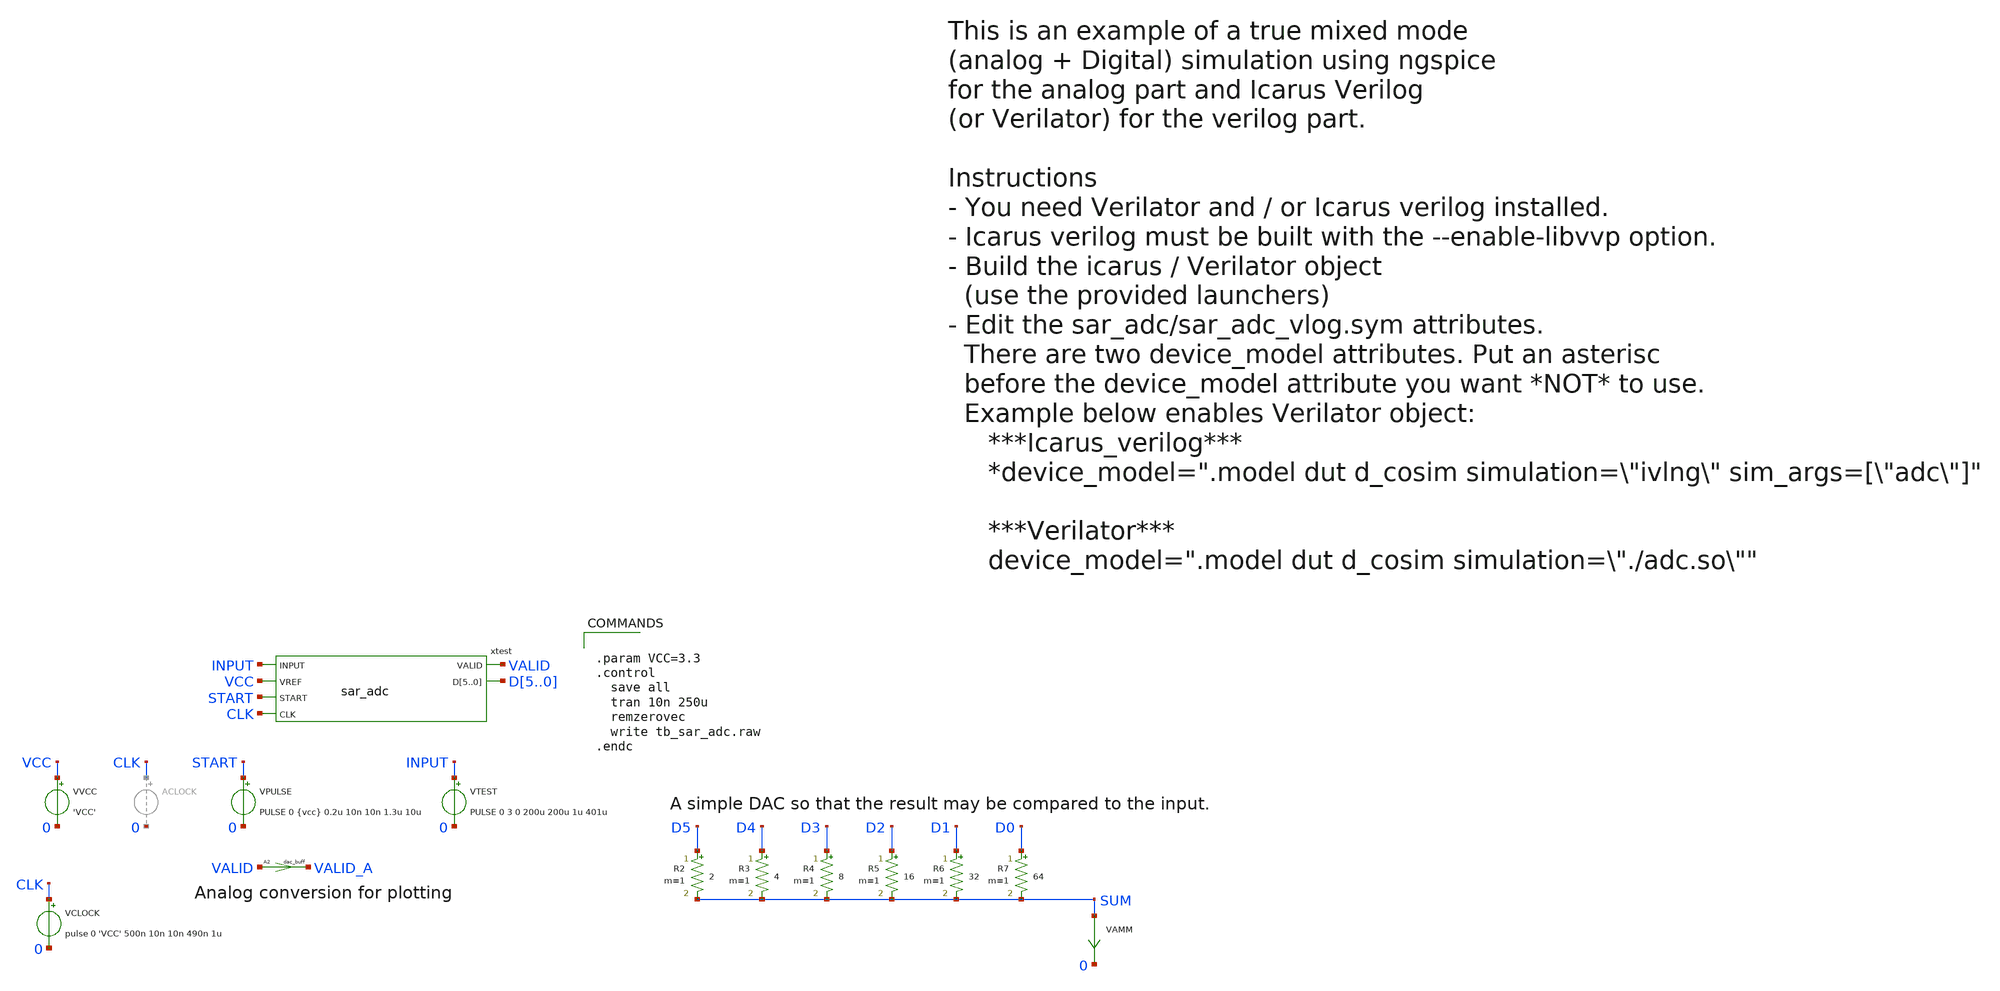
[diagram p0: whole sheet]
** sch_path: xschem_libraries_oa/ngspice_verilog_cosim/tb_sar_adc/schematic/tb_sar_adc.sch
**.subckt tb_sar_adc
VAMM SUM 0 0
VPULSE START 0 PULSE 0 {vcc} 0.2u 10n 10n 1.3u 10u
VTEST INPUT 0 PULSE 0 3 0 200u 200u 1u 401u
VVCC VCC 0 'VCC'
R2 D5 SUM 2 m=1
R3 D4 SUM 4 m=1
R4 D3 SUM 8 m=1
R5 D2 SUM 16 m=1
R6 D1 SUM 32 m=1
R7 D0 SUM 64 m=1
xtest INPUT VCC START VALID D5 D4 D3 D2 D1 D0 CLK sar_adc
A2 [ VALID ] [ VALID_A ] dac_buff
VCLOCK CLK 0 pulse 0 'VCC' 500n 10n 10n 490n 1u
**** begin user architecture code


.param VCC=3.3
.control
  save all
  tran 10n 250u
  remzerovec
  write tb_sar_adc.raw
.endc


**** end user architecture code
**.ends
**** begin user architecture code
.model dac_buff dac_bridge input_load=1e-15 t_rise=10n t_fall=10n  out_low=0 out_high=3.3
**** end user architecture code
.end
